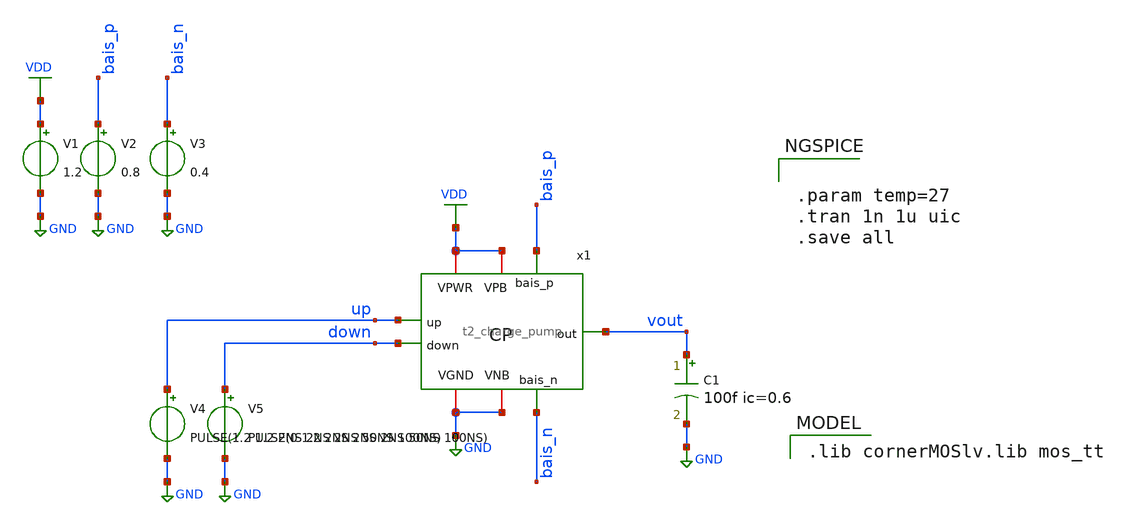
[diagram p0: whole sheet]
** sch_path: Team 2 Design/design_data/xschem/t2_charge_pump_tb.sch
**.subckt t2_charge_pump_tb
x1 VDD VDD GND GND vout up down bais_p bais_n t2_charge_pump
V1 VDD GND 1.2
V2 bais_p GND 0.8
V3 bais_n GND 0.4
V4 up GND PULSE(1.2 1.2 2NS 2NS 2NS 50NS 100NS)
V5 down GND PULSE(0 1.2 2NS 2NS 2NS 50NS 100NS)
C1 vout GND 100f ic=0.6 m=1
**** begin user architecture code


.param temp=27
.tran 1n 1u uic
.save all


 .lib cornerMOSlv.lib mos_tt

**** end user architecture code
**.ends

* expanding   symbol:  t2_charge_pump.sym # of pins=9
** sym_path: Team 2 Design/design_data/xschem/t2_charge_pump.sym
** sch_path: Team 2 Design/design_data/xschem/t2_charge_pump.sch
.subckt t2_charge_pump VPWR VPB VGND VNB out up down bais_p bais_n
*.iopin VPWR
*.ipin up
*.opin out
*.iopin VPB
*.iopin VGND
*.iopin VNB
*.ipin down
*.ipin bais_p
*.ipin bais_n
XM1 i_down bais_n VGND VNB sg13_lv_nmos w=0.15u l=0.13u ng=1 m=1 mm_ok=1
XM2 out down i_down VNB sg13_lv_nmos w=0.15u l=0.13u ng=1 m=1 mm_ok=1
XM3 i_up bais_p VPWR VPB sg13_lv_pmos w=0.3u l=0.13u ng=1 m=1 mm_ok=1
XM4 out up i_up VPB sg13_lv_pmos w=0.3u l=0.13u ng=1 m=1 mm_ok=1
.ends

.GLOBAL GND
.GLOBAL VDD
.end
